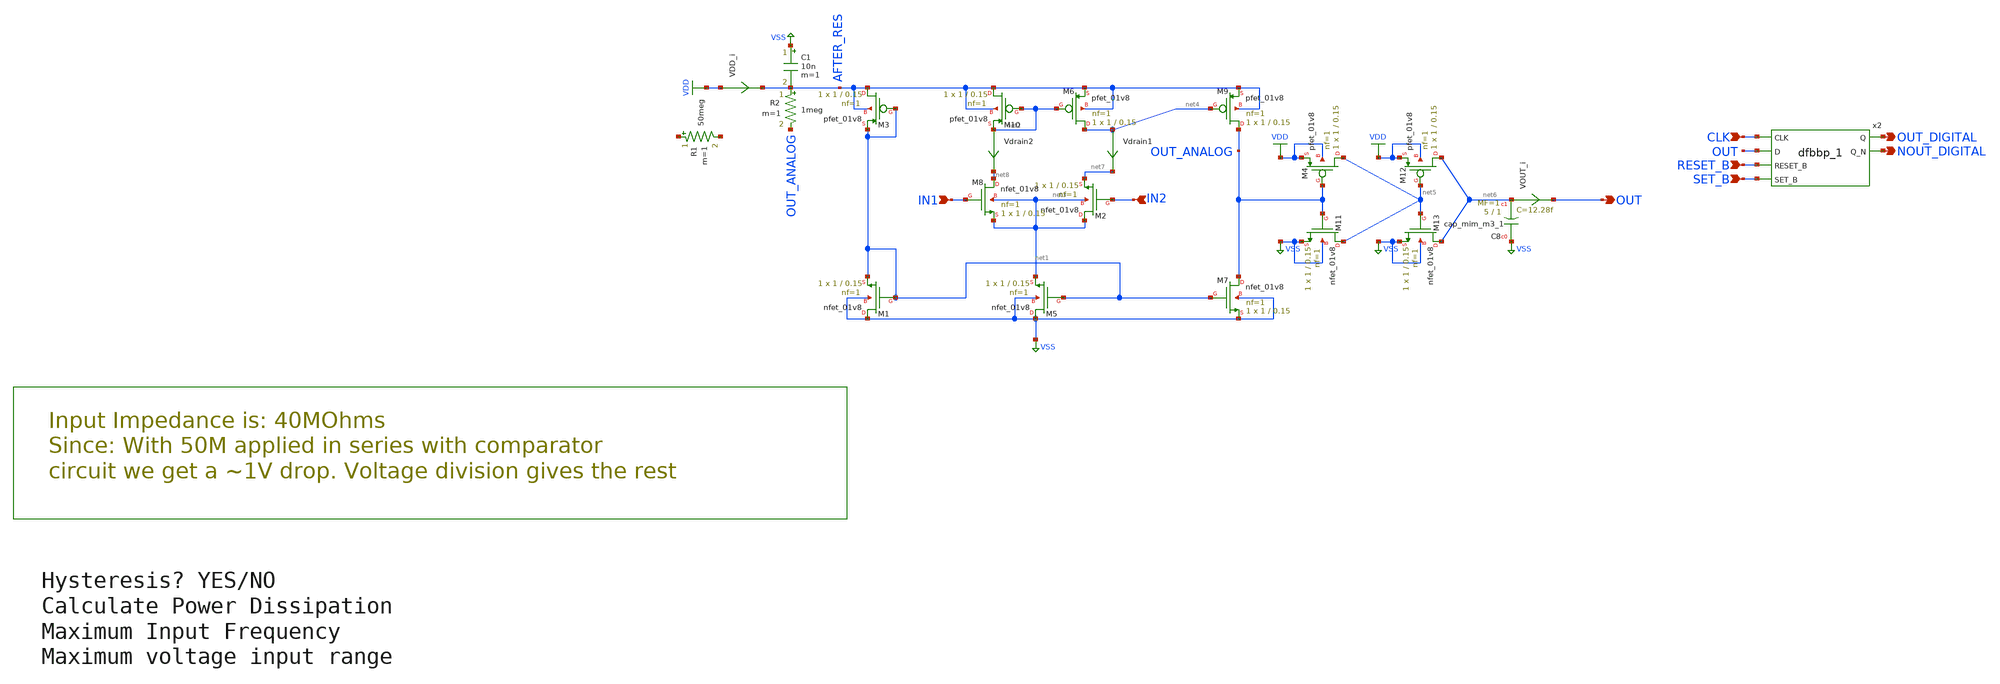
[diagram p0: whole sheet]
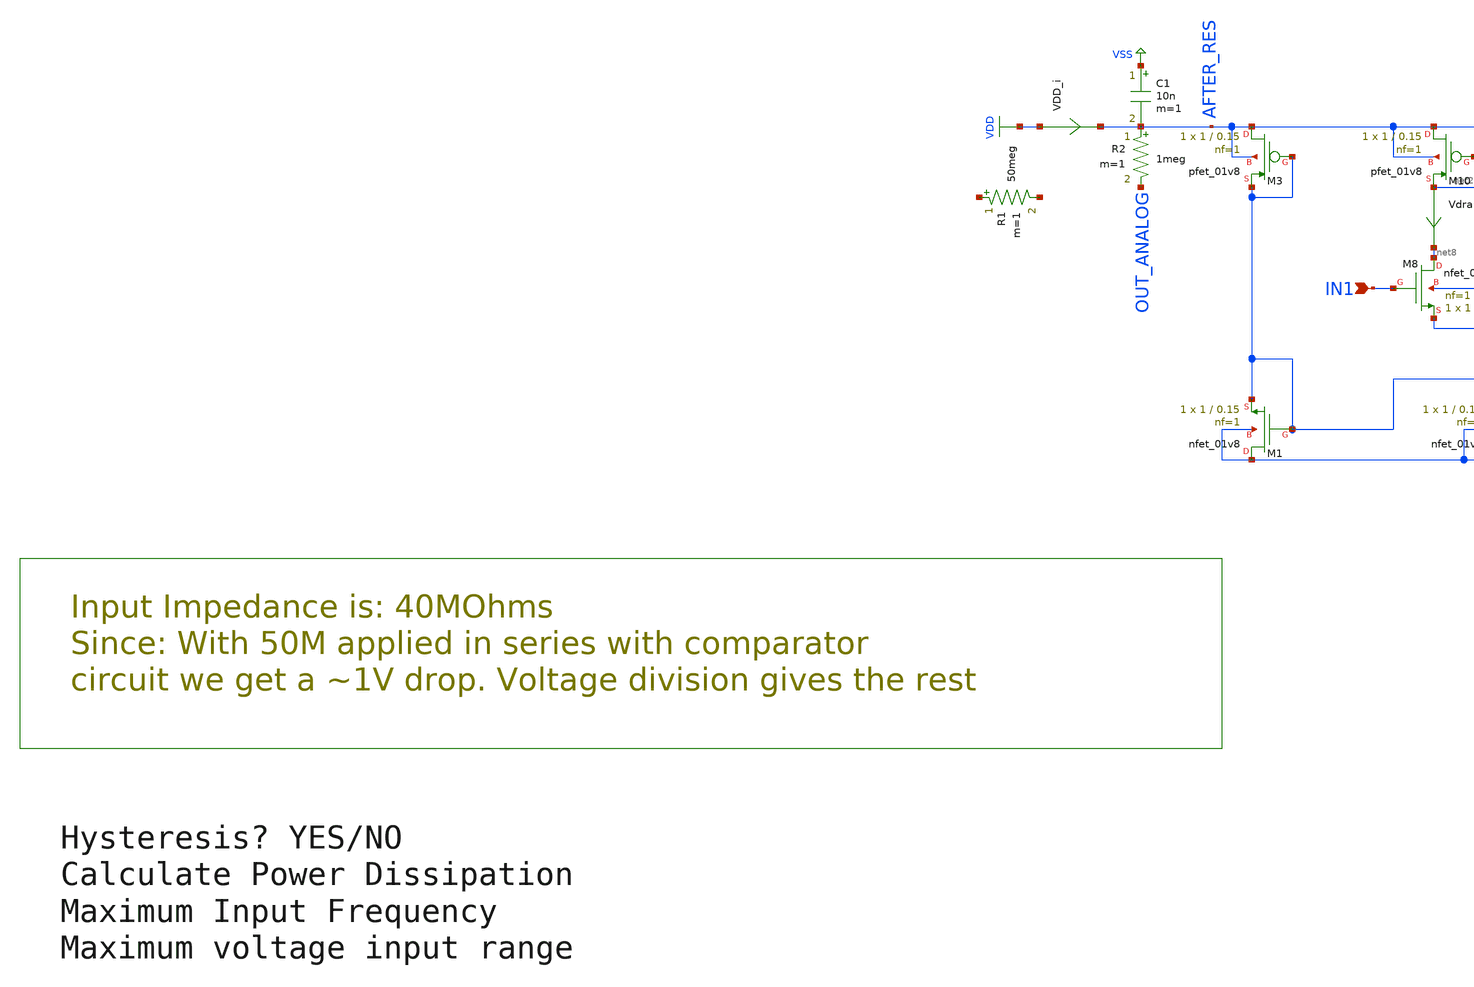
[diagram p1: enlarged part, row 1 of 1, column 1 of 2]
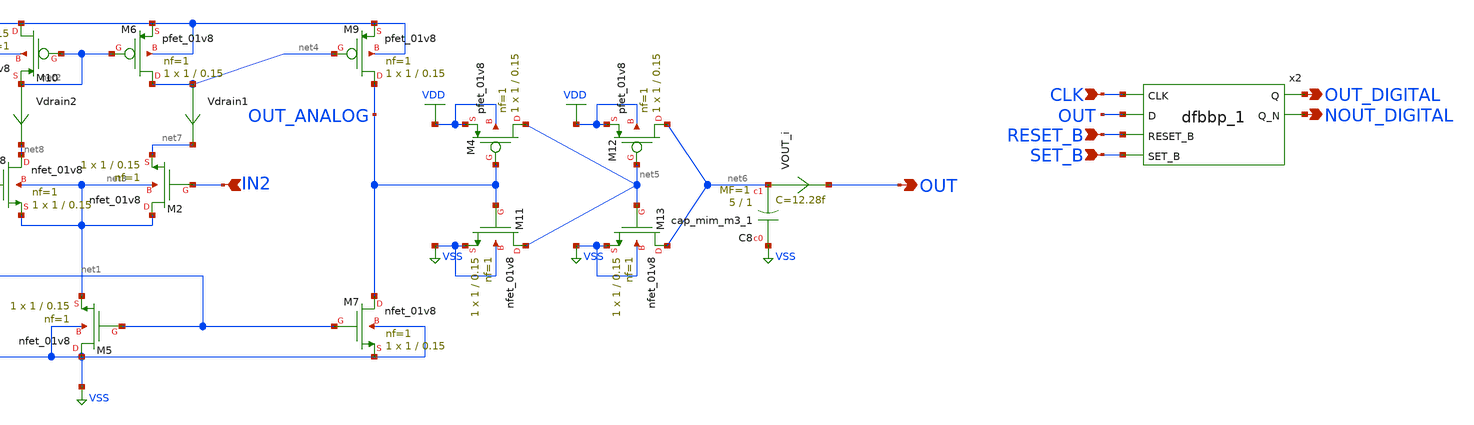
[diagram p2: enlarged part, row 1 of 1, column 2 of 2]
** sch_path: 1bit_adc/1bit_adc.sch
**.subckt 1bit_adc IN1 IN2 OUT OUT_DIGITAL SET_B RESET_B CLK NOUT_DIGITAL
*.ipin IN1
*.ipin IN2
*.opin OUT
*.opin OUT_DIGITAL
*.ipin SET_B
*.ipin RESET_B
*.ipin CLK
*.opin NOUT_DIGITAL
XM9 OUT_ANALOG net4 AFTER_RES AFTER_RES sky130_fd_pr__pfet_01v8 L=0.15 W=1 nf=1 ad='int((nf+1)/2) * W/nf * 0.29'
+ as='int((nf+2)/2) * W/nf * 0.29' pd='2*int((nf+1)/2) * (W/nf + 0.29)' ps='2*int((nf+2)/2) * (W/nf + 0.29)'
+ nrd='0.29 / W' nrs='0.29 / W' sa=0 sb=0 sd=0 mult=1 m=1
XM6 net4 net2 AFTER_RES AFTER_RES sky130_fd_pr__pfet_01v8 L=0.15 W=1 nf=1 ad='int((nf+1)/2) * W/nf * 0.29'
+ as='int((nf+2)/2) * W/nf * 0.29' pd='2*int((nf+1)/2) * (W/nf + 0.29)' ps='2*int((nf+2)/2) * (W/nf + 0.29)'
+ nrd='0.29 / W' nrs='0.29 / W' sa=0 sb=0 sd=0 mult=1 m=1
XM10 AFTER_RES net2 net2 AFTER_RES sky130_fd_pr__pfet_01v8 L=0.15 W=1 nf=1 ad='int((nf+1)/2) * W/nf * 0.29'
+ as='int((nf+2)/2) * W/nf * 0.29' pd='2*int((nf+1)/2) * (W/nf + 0.29)' ps='2*int((nf+2)/2) * (W/nf + 0.29)'
+ nrd='0.29 / W' nrs='0.29 / W' sa=0 sb=0 sd=0 mult=1 m=1
XM3 AFTER_RES net1 net1 AFTER_RES sky130_fd_pr__pfet_01v8 L=0.15 W=1 nf=1 ad='int((nf+1)/2) * W/nf * 0.29'
+ as='int((nf+2)/2) * W/nf * 0.29' pd='2*int((nf+1)/2) * (W/nf + 0.29)' ps='2*int((nf+2)/2) * (W/nf + 0.29)'
+ nrd='0.29 / W' nrs='0.29 / W' sa=0 sb=0 sd=0 mult=1 m=1
XM4 net5 OUT_ANALOG VDD VDD sky130_fd_pr__pfet_01v8 L=0.15 W=1 nf=1 ad='int((nf+1)/2) * W/nf * 0.29'
+ as='int((nf+2)/2) * W/nf * 0.29' pd='2*int((nf+1)/2) * (W/nf + 0.29)' ps='2*int((nf+2)/2) * (W/nf + 0.29)'
+ nrd='0.29 / W' nrs='0.29 / W' sa=0 sb=0 sd=0 mult=1 m=1
XM12 net6 net5 VDD VDD sky130_fd_pr__pfet_01v8 L=0.15 W=1 nf=1 ad='int((nf+1)/2) * W/nf * 0.29' as='int((nf+2)/2) * W/nf * 0.29'
+ pd='2*int((nf+1)/2) * (W/nf + 0.29)' ps='2*int((nf+2)/2) * (W/nf + 0.29)' nrd='0.29 / W' nrs='0.29 / W'
+ sa=0 sb=0 sd=0 mult=1 m=1
Vdrain1 net4 net7 0
.save i(vdrain1)
Vdrain2 net2 net8 0
.save i(vdrain2)
VDD_i VDD AFTER_RES 0
.save i(vdd_i)
VOUT_i net6 OUT 0
.save i(vout_i)
x2 CLK OUT RESET_B SET_B VSS VSS VDD VDD OUT_DIGITAL NOUT_DIGITAL sky130_fd_sc_hd__dfbbp_1
R1 net9 net10 50meg m=1
XM2 net3 IN2 net7 net3 sky130_fd_pr__nfet_01v8 L=0.15 W=1 nf=1 ad='int((nf+1)/2) * W/nf * 0.29' as='int((nf+2)/2) * W/nf * 0.29'
+ pd='2*int((nf+1)/2) * (W/nf + 0.29)' ps='2*int((nf+2)/2) * (W/nf + 0.29)' nrd='0.29 / W' nrs='0.29 / W'
+ sa=0 sb=0 sd=0 mult=1 m=1
XM1 VSS net1 net1 VSS sky130_fd_pr__nfet_01v8 L=0.15 W=1 nf=1 ad='int((nf+1)/2) * W/nf * 0.29' as='int((nf+2)/2) * W/nf * 0.29'
+ pd='2*int((nf+1)/2) * (W/nf + 0.29)' ps='2*int((nf+2)/2) * (W/nf + 0.29)' nrd='0.29 / W' nrs='0.29 / W'
+ sa=0 sb=0 sd=0 mult=1 m=1
XM5 VSS net1 net3 VSS sky130_fd_pr__nfet_01v8 L=0.15 W=1 nf=1 ad='int((nf+1)/2) * W/nf * 0.29' as='int((nf+2)/2) * W/nf * 0.29'
+ pd='2*int((nf+1)/2) * (W/nf + 0.29)' ps='2*int((nf+2)/2) * (W/nf + 0.29)' nrd='0.29 / W' nrs='0.29 / W'
+ sa=0 sb=0 sd=0 mult=1 m=1
XM7 OUT_ANALOG net1 VSS VSS sky130_fd_pr__nfet_01v8 L=0.15 W=1 nf=1 ad='int((nf+1)/2) * W/nf * 0.29'
+ as='int((nf+2)/2) * W/nf * 0.29' pd='2*int((nf+1)/2) * (W/nf + 0.29)' ps='2*int((nf+2)/2) * (W/nf + 0.29)'
+ nrd='0.29 / W' nrs='0.29 / W' sa=0 sb=0 sd=0 mult=1 m=1
XM8 net8 IN1 net3 net3 sky130_fd_pr__nfet_01v8 L=0.15 W=1 nf=1 ad='int((nf+1)/2) * W/nf * 0.29' as='int((nf+2)/2) * W/nf * 0.29'
+ pd='2*int((nf+1)/2) * (W/nf + 0.29)' ps='2*int((nf+2)/2) * (W/nf + 0.29)' nrd='0.29 / W' nrs='0.29 / W'
+ sa=0 sb=0 sd=0 mult=1 m=1
XM11 net5 OUT_ANALOG VSS VSS sky130_fd_pr__nfet_01v8 L=0.15 W=1 nf=1 ad='int((nf+1)/2) * W/nf * 0.29'
+ as='int((nf+2)/2) * W/nf * 0.29' pd='2*int((nf+1)/2) * (W/nf + 0.29)' ps='2*int((nf+2)/2) * (W/nf + 0.29)'
+ nrd='0.29 / W' nrs='0.29 / W' sa=0 sb=0 sd=0 mult=1 m=1
XM13 net6 net5 VSS VSS sky130_fd_pr__nfet_01v8 L=0.15 W=1 nf=1 ad='int((nf+1)/2) * W/nf * 0.29' as='int((nf+2)/2) * W/nf * 0.29'
+ pd='2*int((nf+1)/2) * (W/nf + 0.29)' ps='2*int((nf+2)/2) * (W/nf + 0.29)' nrd='0.29 / W' nrs='0.29 / W'
+ sa=0 sb=0 sd=0 mult=1 m=1
R2 AFTER_RES OUT_ANALOG 1meg m=1
XC8 VSS net6 sky130_fd_pr__cap_mim_m3_1 W=5 L=1 MF=1 m=1
C1 VSS AFTER_RES 10n m=1
**** begin user architecture code


.options gmin=1e-12
.option savecurrents
.option wnflag=1
.param vdd=1.8
.param clk=500n
VVDD VDD 0 DC vdd
VIN1 IN1 0 SIN(1 0.5 450k 5n)
VIN2 IN2 0 SIN(1 0.5 200k 5n)
VGND VSS 0 DC 0
VCLK CLK 0 PULSE(0 {vdd} 0 {clk/8} {clk/8} {clk/2} {clk})
VSET_B SET_B 0 DC vdd
VRESET_B RESET_B 0 DC vdd
.tran {clk/4} {clk*100}

.control
save all
run
remzerovec
write 1bit_adc.raw all

*tran {clk/10} {clk*10}
*plot IN1 IN2
*set appendwrite
*echo AC
*reset
*save all
*ac dec 50 5k 100k
*display
*write 1bit_adc.raw all
echo AMONG US
shell pwd
.endc
.end



** opencircuitdesign pdks install
.lib $::SKYWATER_MODELS/sky130.lib.spice tt
.include $::SKYWATER_STDCELLS/sky130_fd_sc_hd.spice
.include /foss/pdks/sky130A/libs.tech/xschem/sky130_stdcells/
.include /foss/pdks/sky130A/libs.tech/xschem/sky130_fd_pr/

**** end user architecture code
**.ends
.GLOBAL VSS
.GLOBAL VDD
.end
